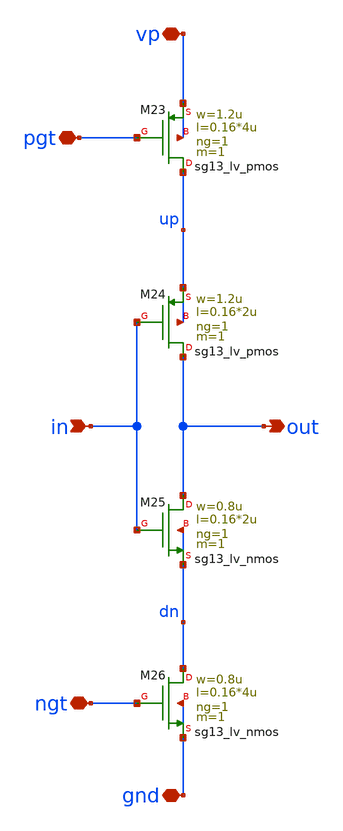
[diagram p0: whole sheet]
** sch_path: schematics/vco/vco_cell/vco_delay_cell_0_meas.sch
**.subckt vco_delay_cell_0_meas in out gnd vp pgt ngt
*.ipin in
*.opin out
*.iopin gnd
*.iopin vp
*.iopin pgt
*.iopin ngt
XM23 up pgt vp vp sg13_lv_pmos w=1.2u l=0.16*4u ng=1 m=1 mm_ok=1
XM24 out in up up sg13_lv_pmos w=1.2u l=0.16*2u ng=1 m=1 mm_ok=1
XM25 out in dn dn sg13_lv_nmos w=0.8u l=0.16*2u ng=1 m=1 mm_ok=1
XM26 dn ngt gnd gnd sg13_lv_nmos w=0.8u l=0.16*4u ng=1 m=1 mm_ok=1
**.ends
.end
